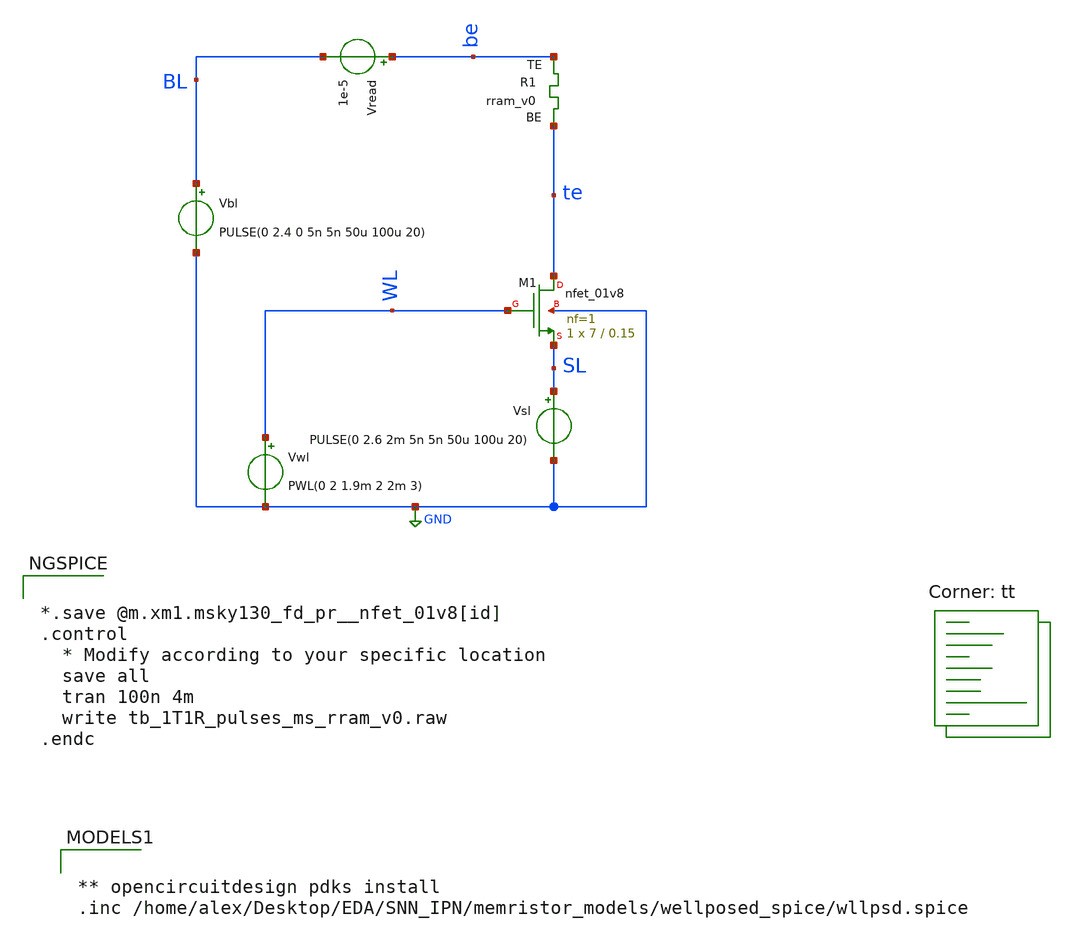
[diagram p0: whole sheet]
** sch_path: memristor_models/wellposed_spice/tb_1T1R_pulses_ms_rram_v0.sch
**.subckt tb_1T1R_pulses_ms_rram_v0
XM1 te WL SL GND sky130_fd_pr__nfet_01v8 L=0.15 W=7 nf=1 ad='int((nf+1)/2) * W/nf * 0.29' as='int((nf+2)/2) * W/nf * 0.29'
+ pd='2*int((nf+1)/2) * (W/nf + 0.29)' ps='2*int((nf+2)/2) * (W/nf + 0.29)' nrd='0.29 / W' nrs='0.29 / W'
+ sa=0 sb=0 sd=0 mult=1 m=1
Vwl WL GND PWL(0 2 1.9m 2 2m 3)
Vbl BL GND PULSE(0 2.4 0 5n 5n 50u 100u 20)
Vread be BL 1e-5
XR1 be te rram_v0
Vsl SL GND PULSE(0 2.6 2m 5n 5n 50u 100u 20)
**** begin user architecture code


*.save @m.xm1.msky130_fd_pr__nfet_01v8[id]
.control
  * Modify according to your specific location
  save all
  tran 100n 4m
  write tb_1T1R_pulses_ms_rram_v0.raw
.endc



.lib $::SKYWATER_MODELS/sky130.lib.spice tt

** opencircuitdesign pdks install
.inc /home/alex/Desktop/EDA/SNN_IPN/memristor_models/wellposed_spice/wllpsd.spice

**** end user architecture code
**.ends
.GLOBAL GND
.end
